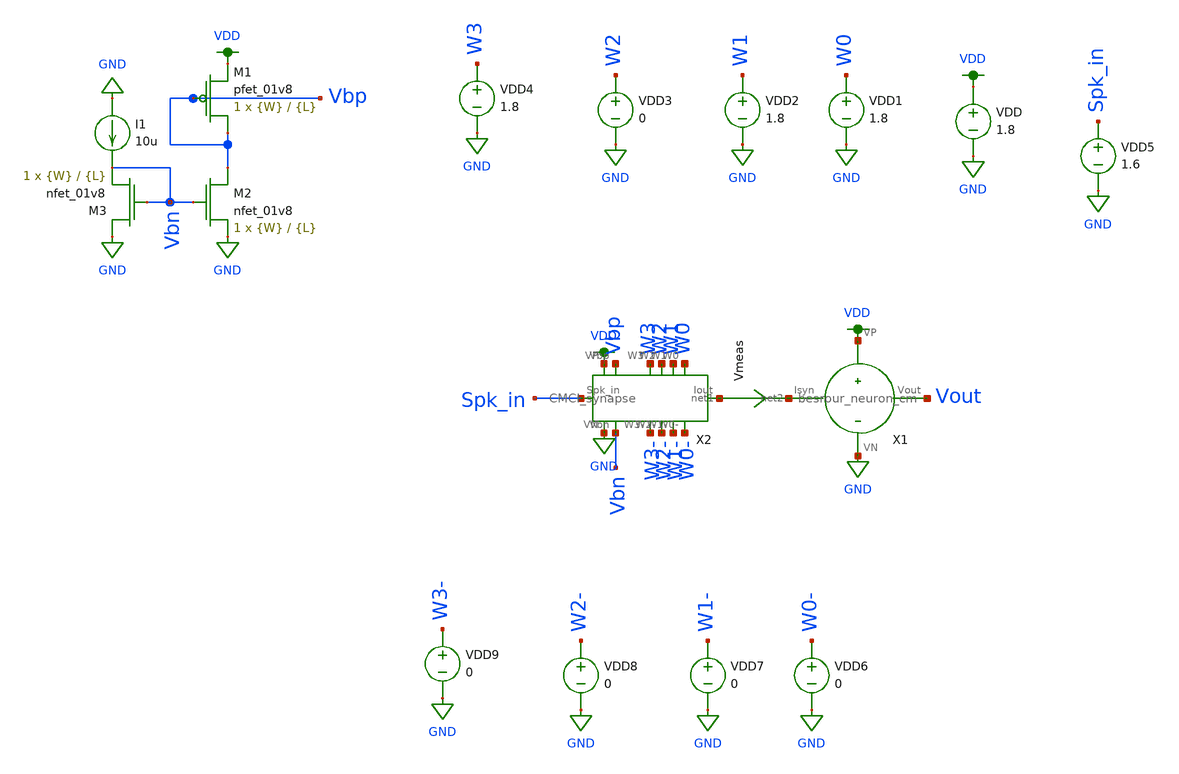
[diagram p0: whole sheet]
** sch_path: schematic/tran_CMCI_show.sch
**.subckt tran_CMCI_show
VDD VDD GND 1.8
VDD1 W0 GND 1.8
VDD2 W1 GND 1.8
VDD3 W2 GND 0
VDD4 W3 GND 1.8
VDD5 Spk_in GND 1.6
Vmeas net1 net2 0
.save i(vmeas)
XM1 Vbp Vbp VDD VDD sky130_fd_pr__pfet_01v8 L={L} W={W} nf=1 ad='int((nf+1)/2) * W/nf * 0.29' as='int((nf+2)/2) * W/nf * 0.29'
+ pd='2*int((nf+1)/2) * (W/nf + 0.29)' ps='2*int((nf+2)/2) * (W/nf + 0.29)' nrd='0.29 / W' nrs='0.29 / W'
+ sa=0 sb=0 sd=0 mult=1 m=1
XM2 Vbp Vbn GND GND sky130_fd_pr__nfet_01v8 L={L} W={W} nf=1 ad='int((nf+1)/2) * W/nf * 0.29' as='int((nf+2)/2) * W/nf * 0.29'
+ pd='2*int((nf+1)/2) * (W/nf + 0.29)' ps='2*int((nf+2)/2) * (W/nf + 0.29)' nrd='0.29 / W' nrs='0.29 / W'
+ sa=0 sb=0 sd=0 mult=1 m=1
XM3 GND Vbn Vbn GND sky130_fd_pr__nfet_01v8 L={L} W={W} nf=1 ad='int((nf+1)/2) * W/nf * 0.29' as='int((nf+2)/2) * W/nf * 0.29'
+ pd='2*int((nf+1)/2) * (W/nf + 0.29)' ps='2*int((nf+2)/2) * (W/nf + 0.29)' nrd='0.29 / W' nrs='0.29 / W'
+ sa=0 sb=0 sd=0 mult=1 m=1
I1 GND Vbn 10u
VDD6 W0- GND 0
VDD7 W1- GND 0
VDD8 W2- GND 0
VDD9 W3- GND 0
X1 net2 Vout VDD GND besrour_neuron_cm
X2 VDD Vbp W3 W2 W1 W0 net1 W0- W1- W2- W3- Vbn GND Spk_in CMCI_synapse
**** begin user architecture code

.param W=2
.param L=0.3
.tran 1ns 10us
.save all



.option wnflag=1
.param MC_SWITCH=0.0
.lib ~/skywater/skywater-pdk/libraries/sky130_fd_pr_ngspice/latest/models/sky130.lib.spice tt

**** end user architecture code
**.ends
.GLOBAL VDD
.GLOBAL GND
.end
